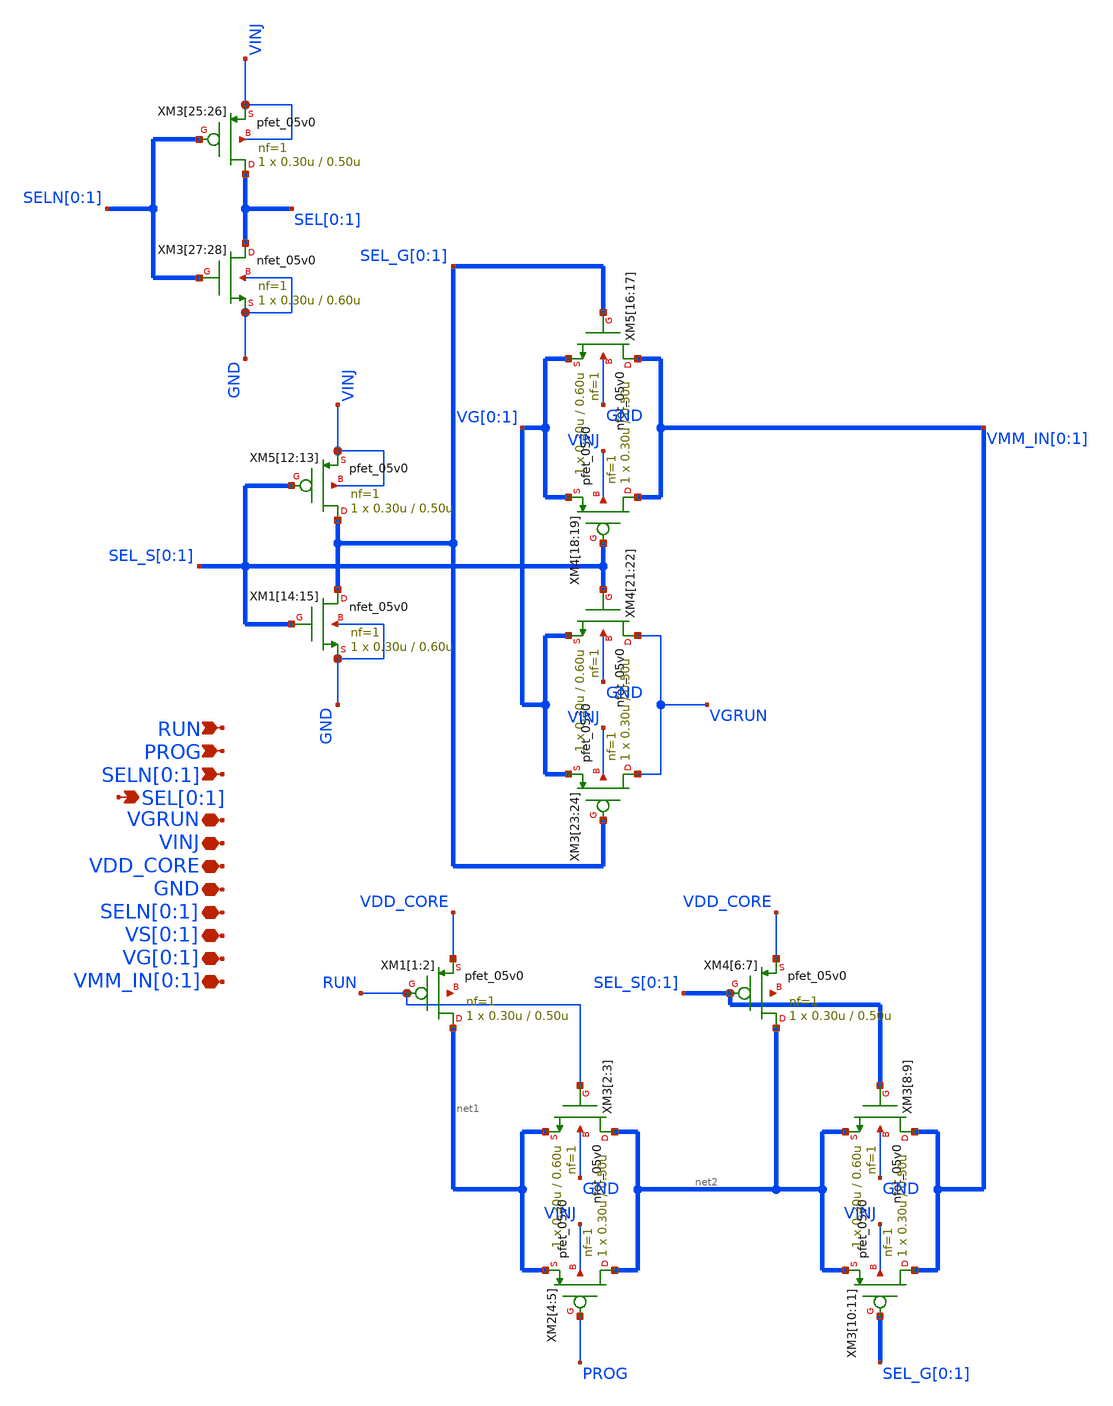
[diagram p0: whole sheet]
** sch_path: 4_Schematics/SWC_GorS.sch
**.subckt SWC_GorS RUN PROG SELN[0],SELN[1] VGRUN VS[0],VS[1] VG[0],VG[1] GND SELN[0],SELN[1] VINJ
*+ VDD_CORE SEL[0],SEL[1] VMM_IN[0],VMM_IN[1]
*.ipin RUN
*.ipin PROG
*.ipin SELN[0],SELN[1]
*.iopin VGRUN
*.iopin VS[0],VS[1]
*.iopin VG[0],VG[1]
*.iopin GND
*.iopin SELN[0],SELN[1]
*.iopin VINJ
*.iopin VDD_CORE
*.opin SEL[0],SEL[1]
*.iopin VMM_IN[0],VMM_IN[1]
XM1[1] net1[1] RUN VDD_CORE net3[1] pfet_05v0 L=0.50u W=0.30u nf=1 ad='int((nf+1)/2) * W/nf * 0.18u'
+ as='int((nf+2)/2) * W/nf * 0.18u' pd='2*int((nf+1)/2) * (W/nf + 0.18u)' ps='2*int((nf+2)/2) * (W/nf + 0.18u)'
+ nrd='0.18u / W' nrs='0.18u / W' sa=0 sb=0 sd=0 m=1
XM1[2] net1[0] RUN VDD_CORE net3[0] pfet_05v0 L=0.50u W=0.30u nf=1 ad='int((nf+1)/2) * W/nf * 0.18u'
+ as='int((nf+2)/2) * W/nf * 0.18u' pd='2*int((nf+1)/2) * (W/nf + 0.18u)' ps='2*int((nf+2)/2) * (W/nf + 0.18u)'
+ nrd='0.18u / W' nrs='0.18u / W' sa=0 sb=0 sd=0 m=1
XM3[2] net2[1] RUN net1[1] GND nfet_05v0 L=0.60u W=0.30u nf=1 ad='int((nf+1)/2) * W/nf * 0.18u' as='int((nf+2)/2) * W/nf * 0.18u'
+ pd='2*int((nf+1)/2) * (W/nf + 0.18u)' ps='2*int((nf+2)/2) * (W/nf + 0.18u)' nrd='0.18u / W' nrs='0.18u / W'
+ sa=0 sb=0 sd=0 m=1
XM3[3] net2[0] RUN net1[0] GND nfet_05v0 L=0.60u W=0.30u nf=1 ad='int((nf+1)/2) * W/nf * 0.18u' as='int((nf+2)/2) * W/nf * 0.18u'
+ pd='2*int((nf+1)/2) * (W/nf + 0.18u)' ps='2*int((nf+2)/2) * (W/nf + 0.18u)' nrd='0.18u / W' nrs='0.18u / W'
+ sa=0 sb=0 sd=0 m=1
XM2[4] net2[1] PROG net1[1] VINJ pfet_05v0 L=0.50u W=0.30u nf=1 ad='int((nf+1)/2) * W/nf * 0.18u' as='int((nf+2)/2) * W/nf * 0.18u'
+ pd='2*int((nf+1)/2) * (W/nf + 0.18u)' ps='2*int((nf+2)/2) * (W/nf + 0.18u)' nrd='0.18u / W' nrs='0.18u / W'
+ sa=0 sb=0 sd=0 m=1
XM2[5] net2[0] PROG net1[0] VINJ pfet_05v0 L=0.50u W=0.30u nf=1 ad='int((nf+1)/2) * W/nf * 0.18u' as='int((nf+2)/2) * W/nf * 0.18u'
+ pd='2*int((nf+1)/2) * (W/nf + 0.18u)' ps='2*int((nf+2)/2) * (W/nf + 0.18u)' nrd='0.18u / W' nrs='0.18u / W'
+ sa=0 sb=0 sd=0 m=1
XM3[8] VMM_IN[0] SEL_S[0] net2[1] GND nfet_05v0 L=0.60u W=0.30u nf=1 ad='int((nf+1)/2) * W/nf * 0.18u'
+ as='int((nf+2)/2) * W/nf * 0.18u' pd='2*int((nf+1)/2) * (W/nf + 0.18u)' ps='2*int((nf+2)/2) * (W/nf + 0.18u)'
+ nrd='0.18u / W' nrs='0.18u / W' sa=0 sb=0 sd=0 m=1
XM3[9] VMM_IN[1] SEL_S[1] net2[0] GND nfet_05v0 L=0.60u W=0.30u nf=1 ad='int((nf+1)/2) * W/nf * 0.18u'
+ as='int((nf+2)/2) * W/nf * 0.18u' pd='2*int((nf+1)/2) * (W/nf + 0.18u)' ps='2*int((nf+2)/2) * (W/nf + 0.18u)'
+ nrd='0.18u / W' nrs='0.18u / W' sa=0 sb=0 sd=0 m=1
XM3[10] VMM_IN[0] SEL_G[0] net2[1] VINJ pfet_05v0 L=0.50u W=0.30u nf=1 ad='int((nf+1)/2) * W/nf * 0.18u'
+ as='int((nf+2)/2) * W/nf * 0.18u' pd='2*int((nf+1)/2) * (W/nf + 0.18u)' ps='2*int((nf+2)/2) * (W/nf + 0.18u)'
+ nrd='0.18u / W' nrs='0.18u / W' sa=0 sb=0 sd=0 m=1
XM3[11] VMM_IN[1] SEL_G[1] net2[0] VINJ pfet_05v0 L=0.50u W=0.30u nf=1 ad='int((nf+1)/2) * W/nf * 0.18u'
+ as='int((nf+2)/2) * W/nf * 0.18u' pd='2*int((nf+1)/2) * (W/nf + 0.18u)' ps='2*int((nf+2)/2) * (W/nf + 0.18u)'
+ nrd='0.18u / W' nrs='0.18u / W' sa=0 sb=0 sd=0 m=1
XM4[6] net2[1] SEL_S[0] VDD_CORE net4[1] pfet_05v0 L=0.50u W=0.30u nf=1 ad='int((nf+1)/2) * W/nf * 0.18u'
+ as='int((nf+2)/2) * W/nf * 0.18u' pd='2*int((nf+1)/2) * (W/nf + 0.18u)' ps='2*int((nf+2)/2) * (W/nf + 0.18u)'
+ nrd='0.18u / W' nrs='0.18u / W' sa=0 sb=0 sd=0 m=1
XM4[7] net2[0] SEL_S[1] VDD_CORE net4[0] pfet_05v0 L=0.50u W=0.30u nf=1 ad='int((nf+1)/2) * W/nf * 0.18u'
+ as='int((nf+2)/2) * W/nf * 0.18u' pd='2*int((nf+1)/2) * (W/nf + 0.18u)' ps='2*int((nf+2)/2) * (W/nf + 0.18u)'
+ nrd='0.18u / W' nrs='0.18u / W' sa=0 sb=0 sd=0 m=1
XM4[21] VGRUN SEL_S[0] VG[0] GND nfet_05v0 L=0.60u W=0.30u nf=1 ad='int((nf+1)/2) * W/nf * 0.18u' as='int((nf+2)/2) * W/nf * 0.18u'
+ pd='2*int((nf+1)/2) * (W/nf + 0.18u)' ps='2*int((nf+2)/2) * (W/nf + 0.18u)' nrd='0.18u / W' nrs='0.18u / W'
+ sa=0 sb=0 sd=0 m=1
XM4[22] VGRUN SEL_S[1] VG[1] GND nfet_05v0 L=0.60u W=0.30u nf=1 ad='int((nf+1)/2) * W/nf * 0.18u' as='int((nf+2)/2) * W/nf * 0.18u'
+ pd='2*int((nf+1)/2) * (W/nf + 0.18u)' ps='2*int((nf+2)/2) * (W/nf + 0.18u)' nrd='0.18u / W' nrs='0.18u / W'
+ sa=0 sb=0 sd=0 m=1
XM3[23] VGRUN SEL_G[0] VG[0] VINJ pfet_05v0 L=0.50u W=0.30u nf=1 ad='int((nf+1)/2) * W/nf * 0.18u' as='int((nf+2)/2) * W/nf * 0.18u'
+ pd='2*int((nf+1)/2) * (W/nf + 0.18u)' ps='2*int((nf+2)/2) * (W/nf + 0.18u)' nrd='0.18u / W' nrs='0.18u / W'
+ sa=0 sb=0 sd=0 m=1
XM3[24] VGRUN SEL_G[1] VG[1] VINJ pfet_05v0 L=0.50u W=0.30u nf=1 ad='int((nf+1)/2) * W/nf * 0.18u' as='int((nf+2)/2) * W/nf * 0.18u'
+ pd='2*int((nf+1)/2) * (W/nf + 0.18u)' ps='2*int((nf+2)/2) * (W/nf + 0.18u)' nrd='0.18u / W' nrs='0.18u / W'
+ sa=0 sb=0 sd=0 m=1
XM5[16] VMM_IN[0] SEL_G[0] VG[0] GND nfet_05v0 L=0.60u W=0.30u nf=1 ad='int((nf+1)/2) * W/nf * 0.18u'
+ as='int((nf+2)/2) * W/nf * 0.18u' pd='2*int((nf+1)/2) * (W/nf + 0.18u)' ps='2*int((nf+2)/2) * (W/nf + 0.18u)'
+ nrd='0.18u / W' nrs='0.18u / W' sa=0 sb=0 sd=0 m=1
XM5[17] VMM_IN[1] SEL_G[1] VG[1] GND nfet_05v0 L=0.60u W=0.30u nf=1 ad='int((nf+1)/2) * W/nf * 0.18u'
+ as='int((nf+2)/2) * W/nf * 0.18u' pd='2*int((nf+1)/2) * (W/nf + 0.18u)' ps='2*int((nf+2)/2) * (W/nf + 0.18u)'
+ nrd='0.18u / W' nrs='0.18u / W' sa=0 sb=0 sd=0 m=1
XM4[18] VMM_IN[0] SEL_S[0] VG[0] VINJ pfet_05v0 L=0.50u W=0.30u nf=1 ad='int((nf+1)/2) * W/nf * 0.18u'
+ as='int((nf+2)/2) * W/nf * 0.18u' pd='2*int((nf+1)/2) * (W/nf + 0.18u)' ps='2*int((nf+2)/2) * (W/nf + 0.18u)'
+ nrd='0.18u / W' nrs='0.18u / W' sa=0 sb=0 sd=0 m=1
XM4[19] VMM_IN[1] SEL_S[1] VG[1] VINJ pfet_05v0 L=0.50u W=0.30u nf=1 ad='int((nf+1)/2) * W/nf * 0.18u'
+ as='int((nf+2)/2) * W/nf * 0.18u' pd='2*int((nf+1)/2) * (W/nf + 0.18u)' ps='2*int((nf+2)/2) * (W/nf + 0.18u)'
+ nrd='0.18u / W' nrs='0.18u / W' sa=0 sb=0 sd=0 m=1
XM1[14] SEL_G[0] SEL_S[0] GND GND nfet_05v0 L=0.60u W=0.30u nf=1 ad='int((nf+1)/2) * W/nf * 0.18u' as='int((nf+2)/2) * W/nf * 0.18u'
+ pd='2*int((nf+1)/2) * (W/nf + 0.18u)' ps='2*int((nf+2)/2) * (W/nf + 0.18u)' nrd='0.18u / W' nrs='0.18u / W'
+ sa=0 sb=0 sd=0 m=1
XM1[15] SEL_G[1] SEL_S[1] GND GND nfet_05v0 L=0.60u W=0.30u nf=1 ad='int((nf+1)/2) * W/nf * 0.18u' as='int((nf+2)/2) * W/nf * 0.18u'
+ pd='2*int((nf+1)/2) * (W/nf + 0.18u)' ps='2*int((nf+2)/2) * (W/nf + 0.18u)' nrd='0.18u / W' nrs='0.18u / W'
+ sa=0 sb=0 sd=0 m=1
XM5[12] SEL_G[0] SEL_S[0] VINJ VINJ pfet_05v0 L=0.50u W=0.30u nf=1 ad='int((nf+1)/2) * W/nf * 0.18u'
+ as='int((nf+2)/2) * W/nf * 0.18u' pd='2*int((nf+1)/2) * (W/nf + 0.18u)' ps='2*int((nf+2)/2) * (W/nf + 0.18u)'
+ nrd='0.18u / W' nrs='0.18u / W' sa=0 sb=0 sd=0 m=1
XM5[13] SEL_G[1] SEL_S[1] VINJ VINJ pfet_05v0 L=0.50u W=0.30u nf=1 ad='int((nf+1)/2) * W/nf * 0.18u'
+ as='int((nf+2)/2) * W/nf * 0.18u' pd='2*int((nf+1)/2) * (W/nf + 0.18u)' ps='2*int((nf+2)/2) * (W/nf + 0.18u)'
+ nrd='0.18u / W' nrs='0.18u / W' sa=0 sb=0 sd=0 m=1
XM3[27] SEL[0] SELN[0] GND GND nfet_05v0 L=0.60u W=0.30u nf=1 ad='int((nf+1)/2) * W/nf * 0.18u' as='int((nf+2)/2) * W/nf * 0.18u'
+ pd='2*int((nf+1)/2) * (W/nf + 0.18u)' ps='2*int((nf+2)/2) * (W/nf + 0.18u)' nrd='0.18u / W' nrs='0.18u / W'
+ sa=0 sb=0 sd=0 m=1
XM3[28] SEL[1] SELN[1] GND GND nfet_05v0 L=0.60u W=0.30u nf=1 ad='int((nf+1)/2) * W/nf * 0.18u' as='int((nf+2)/2) * W/nf * 0.18u'
+ pd='2*int((nf+1)/2) * (W/nf + 0.18u)' ps='2*int((nf+2)/2) * (W/nf + 0.18u)' nrd='0.18u / W' nrs='0.18u / W'
+ sa=0 sb=0 sd=0 m=1
XM3[25] SEL[0] SELN[0] VINJ VINJ pfet_05v0 L=0.50u W=0.30u nf=1 ad='int((nf+1)/2) * W/nf * 0.18u' as='int((nf+2)/2) * W/nf * 0.18u'
+ pd='2*int((nf+1)/2) * (W/nf + 0.18u)' ps='2*int((nf+2)/2) * (W/nf + 0.18u)' nrd='0.18u / W' nrs='0.18u / W'
+ sa=0 sb=0 sd=0 m=1
XM3[26] SEL[1] SELN[1] VINJ VINJ pfet_05v0 L=0.50u W=0.30u nf=1 ad='int((nf+1)/2) * W/nf * 0.18u' as='int((nf+2)/2) * W/nf * 0.18u'
+ pd='2*int((nf+1)/2) * (W/nf + 0.18u)' ps='2*int((nf+2)/2) * (W/nf + 0.18u)' nrd='0.18u / W' nrs='0.18u / W'
+ sa=0 sb=0 sd=0 m=1
**.ends
.end
